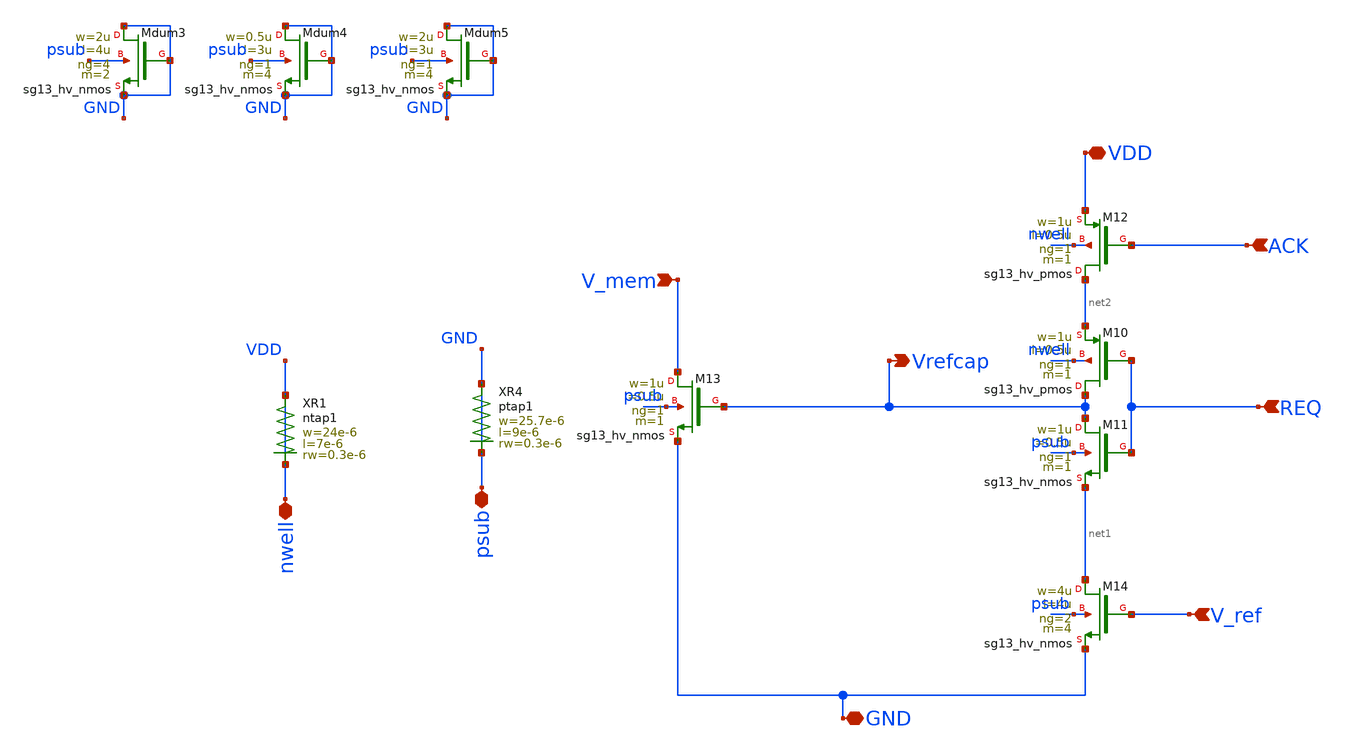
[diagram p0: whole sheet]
** sch_path: xschem/REF_system_BK.sch
**.subckt REF_system_BK VDD GND V_ref REQ ACK V_mem Vrefcap psub nwell
*.iopin VDD
*.iopin GND
*.ipin V_ref
*.ipin REQ
*.ipin ACK
*.ipin V_mem
*.opin Vrefcap
*.iopin psub
*.iopin nwell
XM10 Vrefcap REQ net2 nwell sg13_hv_pmos w=1u l=0.5u ng=1 m=1 mm_ok=1
XM11 Vrefcap REQ net1 psub sg13_hv_nmos w=1u l=0.5u ng=1 m=1 mm_ok=1
XM12 net2 ACK VDD nwell sg13_hv_pmos w=1u l=0.5u ng=1 m=1 mm_ok=1
XM13 V_mem Vrefcap GND psub sg13_hv_nmos w=1u l=0.5u ng=1 m=1 mm_ok=1
XM14 net1 V_ref GND psub sg13_hv_nmos w=4u l=4u ng=2 m=4 mm_ok=1
XMdum3 GND GND GND psub sg13_hv_nmos w=2u l=4u ng=4 m=2 mm_ok=1
XMdum4 GND GND GND psub sg13_hv_nmos w=0.5u l=3u ng=1 m=4 mm_ok=1
XMdum5 GND GND GND psub sg13_hv_nmos w=2u l=3u ng=1 m=4 mm_ok=1
XR4 psub psub ptap1 R=3.342 w=25.7e-6 l=9e-6 rw=0.3e-6
XR1 VDD nwell ntap1 R=3.748 w=24e-6 l=7e-6 rw=0.3e-6
**.ends
.end
